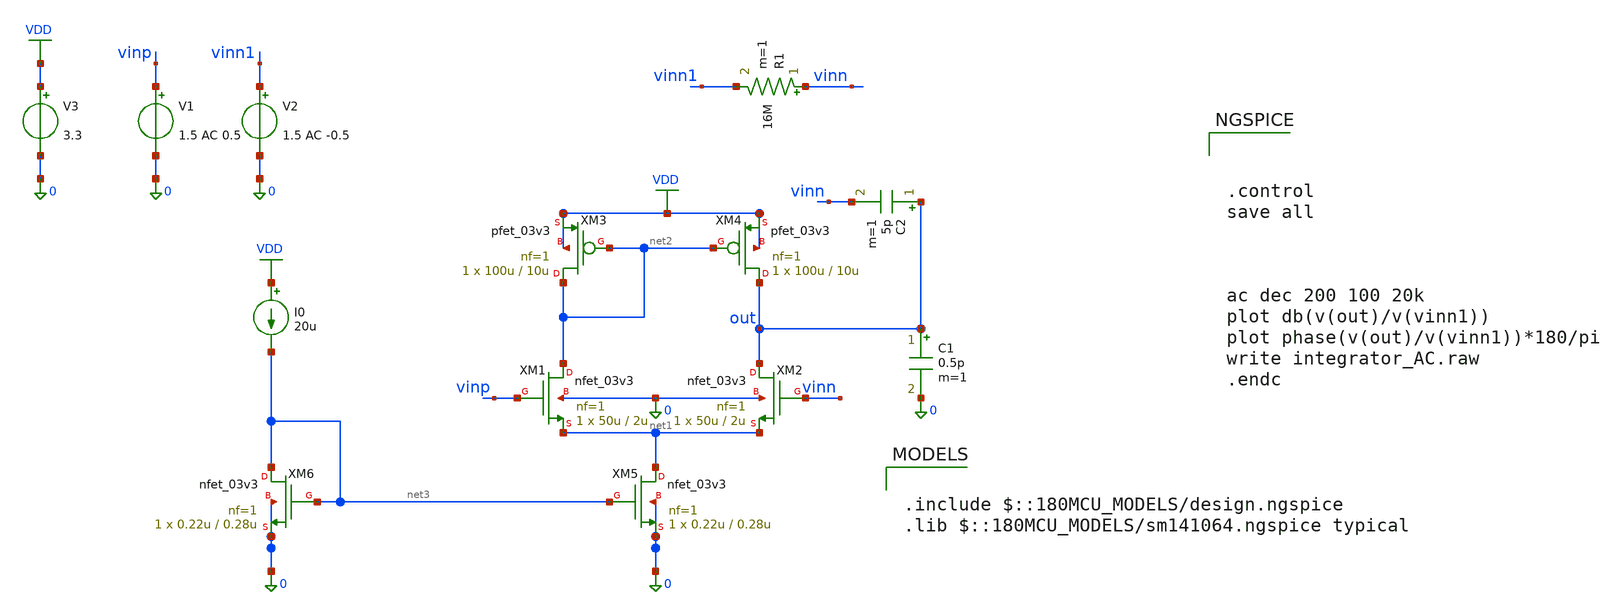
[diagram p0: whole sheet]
** sch_path: integrator/integrator_AC.sch
**.subckt integrator_AC
XM1 net2 vinp net1 0 nfet_03v3 L=2u W=50u nf=1 ad='int((nf+1)/2) * W/nf * 0.18u' as='int((nf+2)/2) * W/nf * 0.18u'
+ pd='2*int((nf+1)/2) * (W/nf + 0.18u)' ps='2*int((nf+2)/2) * (W/nf + 0.18u)' nrd='0.18u / W' nrs='0.18u / W'
+ sa=0 sb=0 sd=0 m=1
XM2 out vinn net1 0 nfet_03v3 L=2u W=50u nf=1 ad='int((nf+1)/2) * W/nf * 0.18u' as='int((nf+2)/2) * W/nf * 0.18u'
+ pd='2*int((nf+1)/2) * (W/nf + 0.18u)' ps='2*int((nf+2)/2) * (W/nf + 0.18u)' nrd='0.18u / W' nrs='0.18u / W'
+ sa=0 sb=0 sd=0 m=1
XM3 net2 net2 VDD VDD pfet_03v3 L=10u W=100u nf=1 ad='int((nf+1)/2) * W/nf * 0.18u' as='int((nf+2)/2) * W/nf * 0.18u'
+ pd='2*int((nf+1)/2) * (W/nf + 0.18u)' ps='2*int((nf+2)/2) * (W/nf + 0.18u)' nrd='0.18u / W' nrs='0.18u / W'
+ sa=0 sb=0 sd=0 m=1
XM4 out net2 VDD VDD pfet_03v3 L=10u W=100u nf=1 ad='int((nf+1)/2) * W/nf * 0.18u' as='int((nf+2)/2) * W/nf * 0.18u'
+ pd='2*int((nf+1)/2) * (W/nf + 0.18u)' ps='2*int((nf+2)/2) * (W/nf + 0.18u)' nrd='0.18u / W' nrs='0.18u / W'
+ sa=0 sb=0 sd=0 m=1
XM5 net1 net3 0 0 nfet_03v3 L=0.28u W=0.22u nf=1 ad='int((nf+1)/2) * W/nf * 0.18u' as='int((nf+2)/2) * W/nf * 0.18u'
+ pd='2*int((nf+1)/2) * (W/nf + 0.18u)' ps='2*int((nf+2)/2) * (W/nf + 0.18u)' nrd='0.18u / W' nrs='0.18u / W'
+ sa=0 sb=0 sd=0 m=1
XM6 net3 net3 0 0 nfet_03v3 L=0.28u W=0.22u nf=1 ad='int((nf+1)/2) * W/nf * 0.18u' as='int((nf+2)/2) * W/nf * 0.18u'
+ pd='2*int((nf+1)/2) * (W/nf + 0.18u)' ps='2*int((nf+2)/2) * (W/nf + 0.18u)' nrd='0.18u / W' nrs='0.18u / W'
+ sa=0 sb=0 sd=0 m=1
V1 vinp 0 1.5 AC 0.5
V2 vinn1 0 1.5 AC -0.5
V3 VDD 0 3.3
C1 out 0 0.5p m=1
I0 VDD net3 20u
C2 out vinn 5p m=1
R1 vinn vinn1 16M m=1
**** begin user architecture code

.include $::180MCU_MODELS/design.ngspice
.lib $::180MCU_MODELS/sm141064.ngspice typical




.control
save all



ac dec 200 100 20k
plot db(v(out)/v(vinn1))
plot phase(v(out)/v(vinn1))*180/pi
write integrator_AC.raw
.endc


**** end user architecture code
**.ends
.GLOBAL VDD
.end
